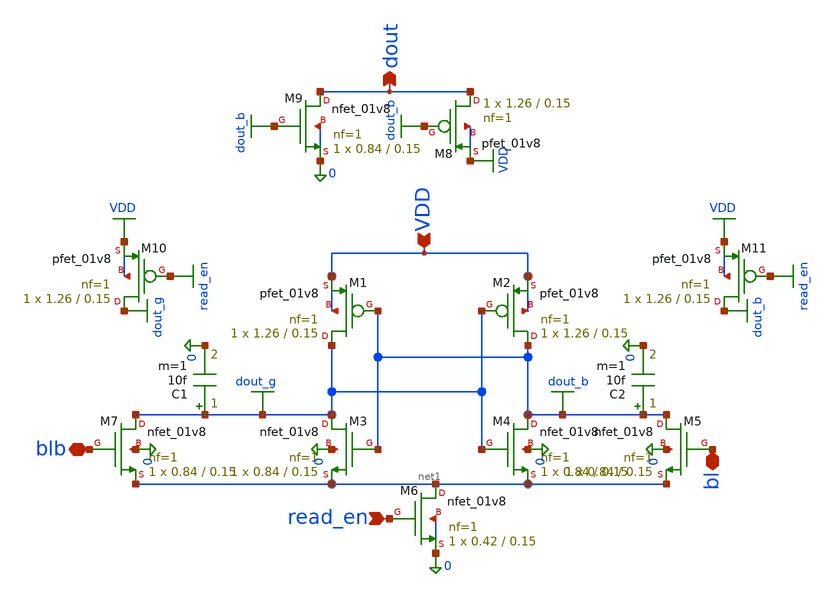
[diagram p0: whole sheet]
** sch_path: xschem/Subcircuits/sense_amplifier.sch
**.subckt sense_amplifier VDD bl blb read_en dout
*.ipin VDD
*.iopin bl
*.iopin blb
*.ipin read_en
*.opin dout
XM1 dout_g dout_b VDD VDD sky130_fd_pr__pfet_01v8 L=0.15 W=1.26 nf=1 ad='int((1 + 1)/2) * 1.26 / 1 * 0.29'
+ as='int((1 + 2)/2) * 1.26 / 1 * 0.29' pd='2*int((1 + 1)/2) * (1.26 / 1 + 0.29)' ps='2*int((1 + 2)/2) * (1.26 / 1 + 0.29)'
+ nrd='0.29 / 1.26 ' nrs='0.29 / 1.26 ' sa=0 sb=0 sd=0 mult=1 m=1
XM2 dout_b dout_g VDD VDD sky130_fd_pr__pfet_01v8 L=0.15 W=1.26 nf=1 ad='int((1 + 1)/2) * 1.26 / 1 * 0.29'
+ as='int((1 + 2)/2) * 1.26 / 1 * 0.29' pd='2*int((1 + 1)/2) * (1.26 / 1 + 0.29)' ps='2*int((1 + 2)/2) * (1.26 / 1 + 0.29)'
+ nrd='0.29 / 1.26 ' nrs='0.29 / 1.26 ' sa=0 sb=0 sd=0 mult=1 m=1
XM3 dout_g dout_b net1 0 sky130_fd_pr__nfet_01v8 L=0.15 W=0.84 nf=1 ad='int((1 + 1)/2) * 0.84 / 1 * 0.29'
+ as='int((1 + 2)/2) * 0.84 / 1 * 0.29' pd='2*int((1 + 1)/2) * (0.84 / 1 + 0.29)' ps='2*int((1 + 2)/2) * (0.84 / 1 + 0.29)'
+ nrd='0.29 / 0.84 ' nrs='0.29 / 0.84 ' sa=0 sb=0 sd=0 mult=1 m=1
XM4 dout_b dout_g net1 0 sky130_fd_pr__nfet_01v8 L=0.15 W=0.84 nf=1 ad='int((1 + 1)/2) * 0.84 / 1 * 0.29'
+ as='int((1 + 2)/2) * 0.84 / 1 * 0.29' pd='2*int((1 + 1)/2) * (0.84 / 1 + 0.29)' ps='2*int((1 + 2)/2) * (0.84 / 1 + 0.29)'
+ nrd='0.29 / 0.84 ' nrs='0.29 / 0.84 ' sa=0 sb=0 sd=0 mult=1 m=1
XM5 dout_b bl net1 0 sky130_fd_pr__nfet_01v8 L=0.15 W=0.84 nf=1 ad='int((1 + 1)/2) * 0.84 / 1 * 0.29'
+ as='int((1 + 2)/2) * 0.84 / 1 * 0.29' pd='2*int((1 + 1)/2) * (0.84 / 1 + 0.29)' ps='2*int((1 + 2)/2) * (0.84 / 1 + 0.29)'
+ nrd='0.29 / 0.84 ' nrs='0.29 / 0.84 ' sa=0 sb=0 sd=0 mult=1 m=1
XM7 dout_g blb net1 0 sky130_fd_pr__nfet_01v8 L=0.15 W=0.84 nf=1 ad='int((1 + 1)/2) * 0.84 / 1 * 0.29'
+ as='int((1 + 2)/2) * 0.84 / 1 * 0.29' pd='2*int((1 + 1)/2) * (0.84 / 1 + 0.29)' ps='2*int((1 + 2)/2) * (0.84 / 1 + 0.29)'
+ nrd='0.29 / 0.84 ' nrs='0.29 / 0.84 ' sa=0 sb=0 sd=0 mult=1 m=1
XM6 net1 read_en 0 0 sky130_fd_pr__nfet_01v8 L=0.15 W=0.42 nf=1 ad='int((1 + 1)/2) * 0.42 / 1 * 0.29'
+ as='int((1 + 2)/2) * 0.42 / 1 * 0.29' pd='2*int((1 + 1)/2) * (0.42 / 1 + 0.29)' ps='2*int((1 + 2)/2) * (0.42 / 1 + 0.29)'
+ nrd='0.29 / 0.42 ' nrs='0.29 / 0.42 ' sa=0 sb=0 sd=0 mult=1 m=1
C1 dout_g 0 10f m=1
C2 dout_b 0 10f m=1
XM10 dout_g read_en VDD VDD sky130_fd_pr__pfet_01v8 L=0.15 W=1.26 nf=1 ad='int((1 + 1)/2) * 1.26 / 1 * 0.29'
+ as='int((1 + 2)/2) * 1.26 / 1 * 0.29' pd='2*int((1 + 1)/2) * (1.26 / 1 + 0.29)' ps='2*int((1 + 2)/2) * (1.26 / 1 + 0.29)'
+ nrd='0.29 / 1.26 ' nrs='0.29 / 1.26 ' sa=0 sb=0 sd=0 mult=1 m=1
XM11 dout_b read_en VDD VDD sky130_fd_pr__pfet_01v8 L=0.15 W=1.26 nf=1 ad='int((1 + 1)/2) * 1.26 / 1 * 0.29'
+ as='int((1 + 2)/2) * 1.26 / 1 * 0.29' pd='2*int((1 + 1)/2) * (1.26 / 1 + 0.29)' ps='2*int((1 + 2)/2) * (1.26 / 1 + 0.29)'
+ nrd='0.29 / 1.26 ' nrs='0.29 / 1.26 ' sa=0 sb=0 sd=0 mult=1 m=1
XM8 dout dout_b VDD VDD sky130_fd_pr__pfet_01v8 L=0.15 W=1.26 nf=1 ad='int((1 + 1)/2) * 1.26 / 1 * 0.29'
+ as='int((1 + 2)/2) * 1.26 / 1 * 0.29' pd='2*int((1 + 1)/2) * (1.26 / 1 + 0.29)' ps='2*int((1 + 2)/2) * (1.26 / 1 + 0.29)'
+ nrd='0.29 / 1.26 ' nrs='0.29 / 1.26 ' sa=0 sb=0 sd=0 mult=1 m=1
XM9 dout dout_b 0 0 sky130_fd_pr__nfet_01v8 L=0.15 W=0.84 nf=1 ad='int((1 + 1)/2) * 0.84 / 1 * 0.29'
+ as='int((1 + 2)/2) * 0.84 / 1 * 0.29' pd='2*int((1 + 1)/2) * (0.84 / 1 + 0.29)' ps='2*int((1 + 2)/2) * (0.84 / 1 + 0.29)'
+ nrd='0.29 / 0.84 ' nrs='0.29 / 0.84 ' sa=0 sb=0 sd=0 mult=1 m=1
**.ends
.GLOBAL dout_b
.GLOBAL dout_g
.GLOBAL read_en
.GLOBAL VDD
.end
